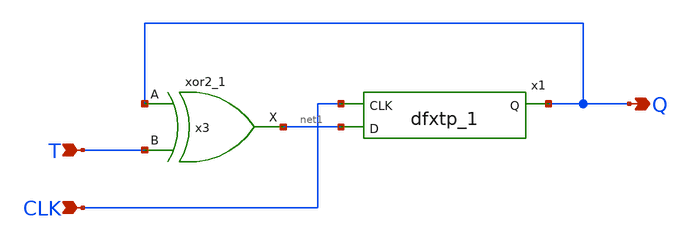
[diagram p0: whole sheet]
** sch_path: xschem/T_flip_flop/t_ff_sc_lp.sch
**.subckt t_ff_sc_lp T CLK Q
*.ipin T
*.ipin CLK
*.opin Q
x3 Q T GND GND VDD VDD net1 sky130_fd_sc_lp__xor2_1
x1 CLK net1 GND GND VDD VDD Q sky130_fd_sc_lp__dfxtp_1
**.ends
.end
